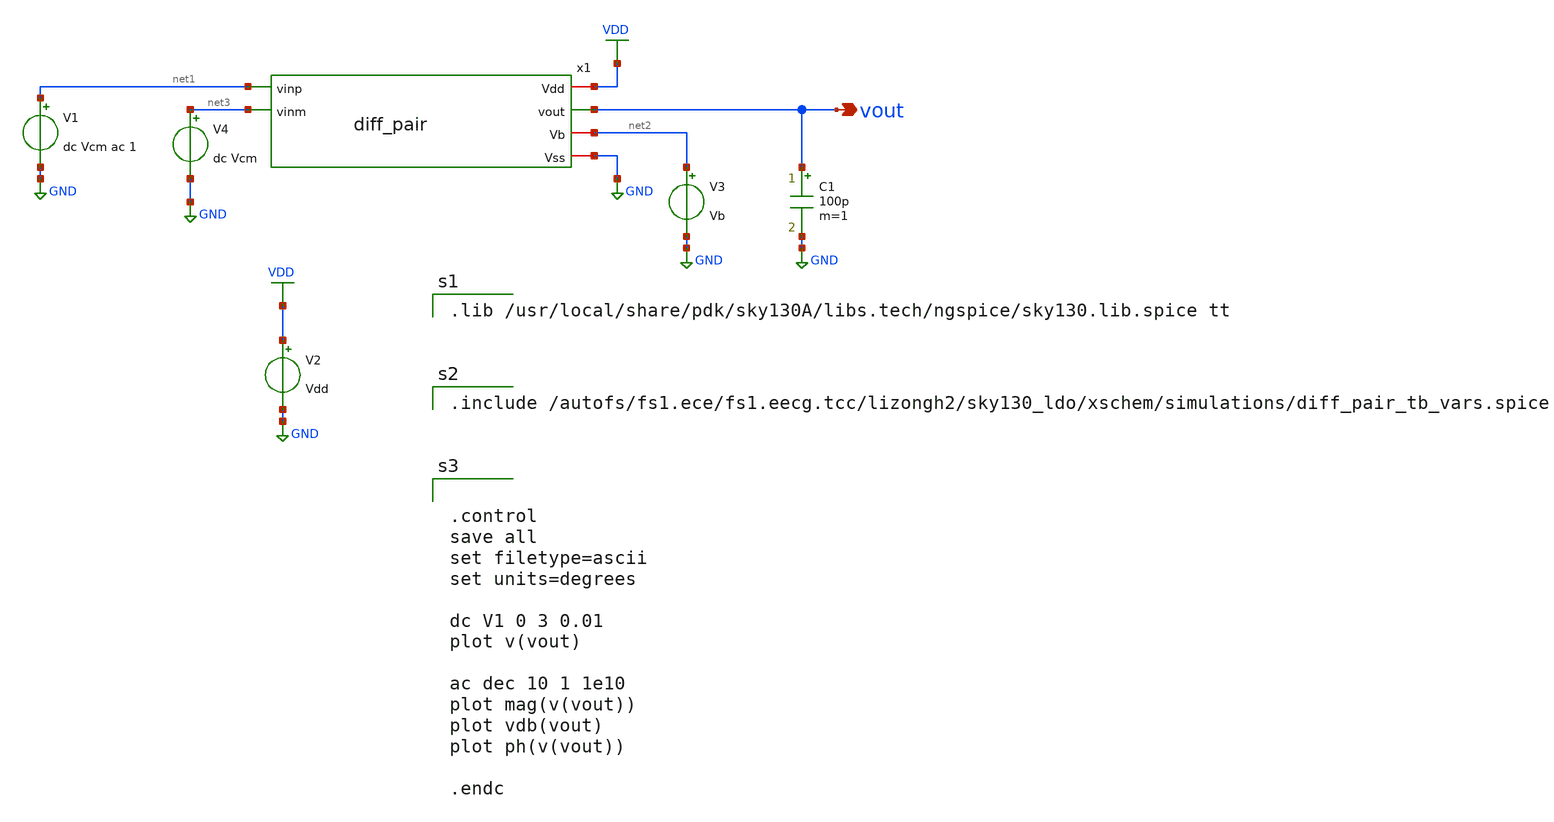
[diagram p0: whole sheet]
** sch_path: xschem/diff_pair_tb.sch
**.subckt diff_pair_tb vout
*.opin vout
V1 net1 GND dc Vcm ac 1
V2 VDD GND Vdd
V3 net2 GND Vb
C1 vout GND 100p m=1
V4 net3 GND dc Vcm
x1 VDD vout net1 net3 net2 GND diff_pair
**** begin user architecture code

.lib /usr/local/share/pdk/sky130A/libs.tech/ngspice/sky130.lib.spice tt


.include /autofs/fs1.ece/fs1.eecg.tcc/lizongh2/sky130_ldo/xschem/simulations/diff_pair_tb_vars.spice




.control
save all
set filetype=ascii
set units=degrees

dc V1 0 3 0.01
plot v(vout)

ac dec 10 1 1e10
plot mag(v(vout))
plot vdb(vout)
plot ph(v(vout))

.endc


**** end user architecture code
**.ends

* expanding   symbol:  diff_pair.sym # of pins=6
** sym_path: xschem/diff_pair.sym
** sch_path: xschem/diff_pair.sch
.subckt diff_pair Vdd vout vinp vinm Vb Vss
*.iopin Vdd
*.ipin vinm
*.ipin vinp
*.iopin Vb
*.opin vout
*.iopin Vss
XM1 net1 vinp net2 Vss sky130_fd_pr__nfet_g5v0d10v5 L=L_M1 W=W_M1 nf=1 ad='int((nf+1)/2) * W/nf * 0.29'
+ as='int((nf+2)/2) * W/nf * 0.29' pd='2*int((nf+1)/2) * (W/nf + 0.29)' ps='2*int((nf+2)/2) * (W/nf + 0.29)'
+ nrd='0.29 / W' nrs='0.29 / W' sa=0 sb=0 sd=0 mult=1 m=1
XM2 vout vinm net2 Vss sky130_fd_pr__nfet_g5v0d10v5 L=L_M2 W=W_M2 nf=1 ad='int((nf+1)/2) * W/nf * 0.29'
+ as='int((nf+2)/2) * W/nf * 0.29' pd='2*int((nf+1)/2) * (W/nf + 0.29)' ps='2*int((nf+2)/2) * (W/nf + 0.29)'
+ nrd='0.29 / W' nrs='0.29 / W' sa=0 sb=0 sd=0 mult=1 m=1
XM3 vout net1 Vdd Vdd sky130_fd_pr__pfet_g5v0d10v5 L=L_M3 W=W_M3 nf=1 ad='int((nf+1)/2) * W/nf * 0.29'
+ as='int((nf+2)/2) * W/nf * 0.29' pd='2*int((nf+1)/2) * (W/nf + 0.29)' ps='2*int((nf+2)/2) * (W/nf + 0.29)'
+ nrd='0.29 / W' nrs='0.29 / W' sa=0 sb=0 sd=0 mult=1 m=1
XM4 net1 net1 Vdd Vdd sky130_fd_pr__pfet_g5v0d10v5 L=L_M4 W=W_M4 nf=1 ad='int((nf+1)/2) * W/nf * 0.29'
+ as='int((nf+2)/2) * W/nf * 0.29' pd='2*int((nf+1)/2) * (W/nf + 0.29)' ps='2*int((nf+2)/2) * (W/nf + 0.29)'
+ nrd='0.29 / W' nrs='0.29 / W' sa=0 sb=0 sd=0 mult=1 m=1
XM5 net2 Vb Vss Vss sky130_fd_pr__nfet_g5v0d10v5 L=L_M5 W=W_M5 nf=1 ad='int((nf+1)/2) * W/nf * 0.29'
+ as='int((nf+2)/2) * W/nf * 0.29' pd='2*int((nf+1)/2) * (W/nf + 0.29)' ps='2*int((nf+2)/2) * (W/nf + 0.29)'
+ nrd='0.29 / W' nrs='0.29 / W' sa=0 sb=0 sd=0 mult=1 m=1
.ends

.GLOBAL GND
.GLOBAL VDD
.end
